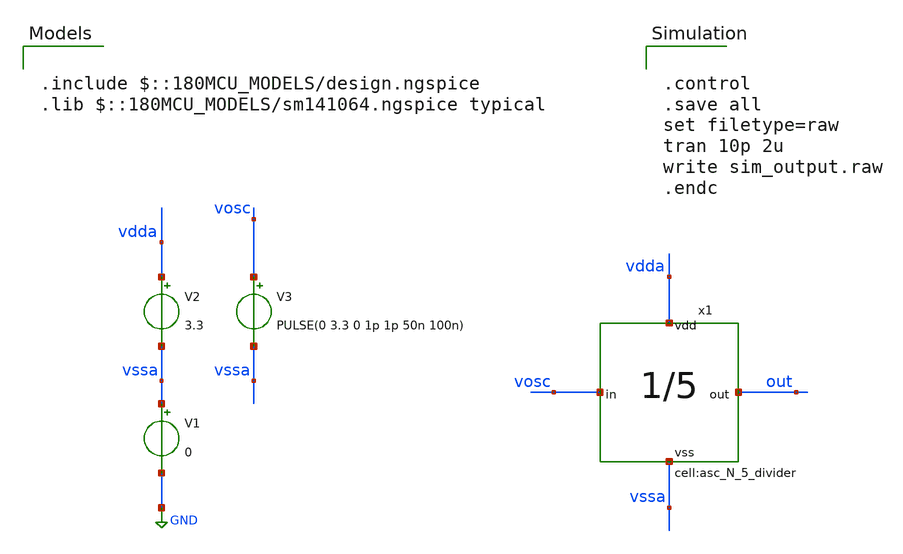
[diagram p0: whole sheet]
** sch_path: designs/libs/tb_analog/tb_asc_N_5_divider/tb_asc_N_5_divider.sch
**.subckt tb_asc_N_5_divider
V1 vssa GND 0
V2 vdda vssa 3.3
V3 vosc vssa PULSE(0 3.3 0 1p 1p 50n 100n)
x1 vosc out vdda vssa asc_N_5_divider
**** begin user architecture code

.include $::180MCU_MODELS/design.ngspice
.lib $::180MCU_MODELS/sm141064.ngspice typical



.control
.save all
set filetype=raw
tran 10p 2u
write sim_output.raw
.endc


**** end user architecture code
**.ends
.GLOBAL GND
.end
